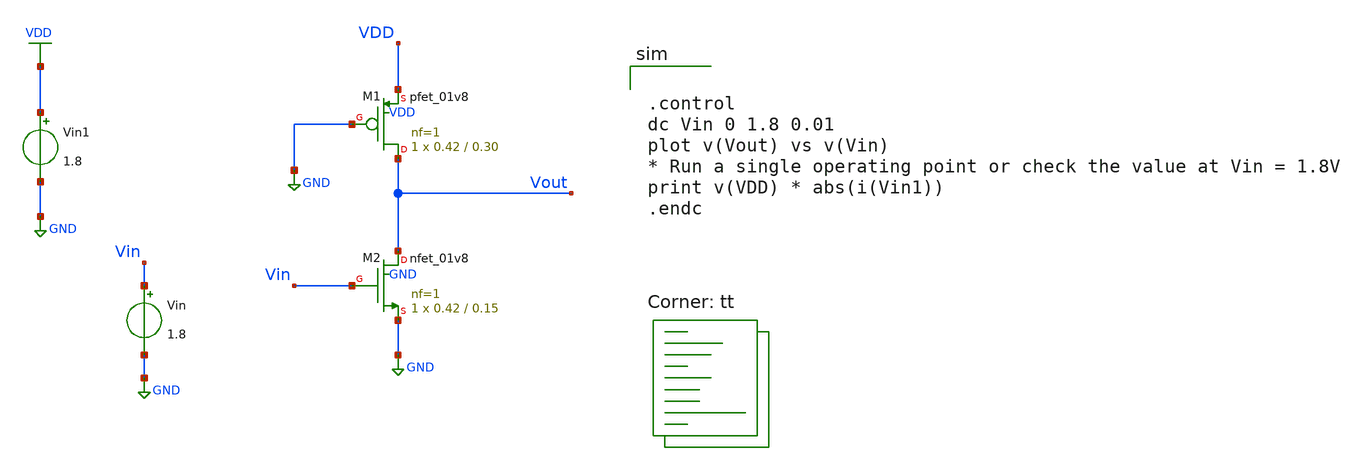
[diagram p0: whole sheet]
** sch_path: assignments/assignment2/assign2c.sch
**.subckt assign2c
XM1 Vout GND VDD VDD sky130_fd_pr__pfet_01v8 L=0.30 W=0.42 nf=1 ad='int((nf+1)/2) * W/nf * 0.29' as='int((nf+2)/2) * W/nf * 0.29'
+ pd='2*int((nf+1)/2) * (W/nf + 0.29)' ps='2*int((nf+2)/2) * (W/nf + 0.29)' nrd='0.29 / W' nrs='0.29 / W'
+ sa=0 sb=0 sd=0 mult=1 m=1
XM2 Vout Vin GND GND sky130_fd_pr__nfet_01v8 L=0.15 W=0.42 nf=1 ad='int((nf+1)/2) * W/nf * 0.29' as='int((nf+2)/2) * W/nf * 0.29'
+ pd='2*int((nf+1)/2) * (W/nf + 0.29)' ps='2*int((nf+2)/2) * (W/nf + 0.29)' nrd='0.29 / W' nrs='0.29 / W'
+ sa=0 sb=0 sd=0 mult=1 m=1
Vin1 VDD GND 1.8
Vin Vin GND 1.8
**** begin user architecture code


.control
dc Vin 0 1.8 0.01
plot v(Vout) vs v(Vin)
* Run a single operating point or check the value at Vin = 1.8V
print v(VDD) * abs(i(Vin1))
.endc


.lib $::SKYWATER_MODELS/sky130.lib.spice tt
**** end user architecture code
**.ends
.GLOBAL GND
.GLOBAL VDD
.end
